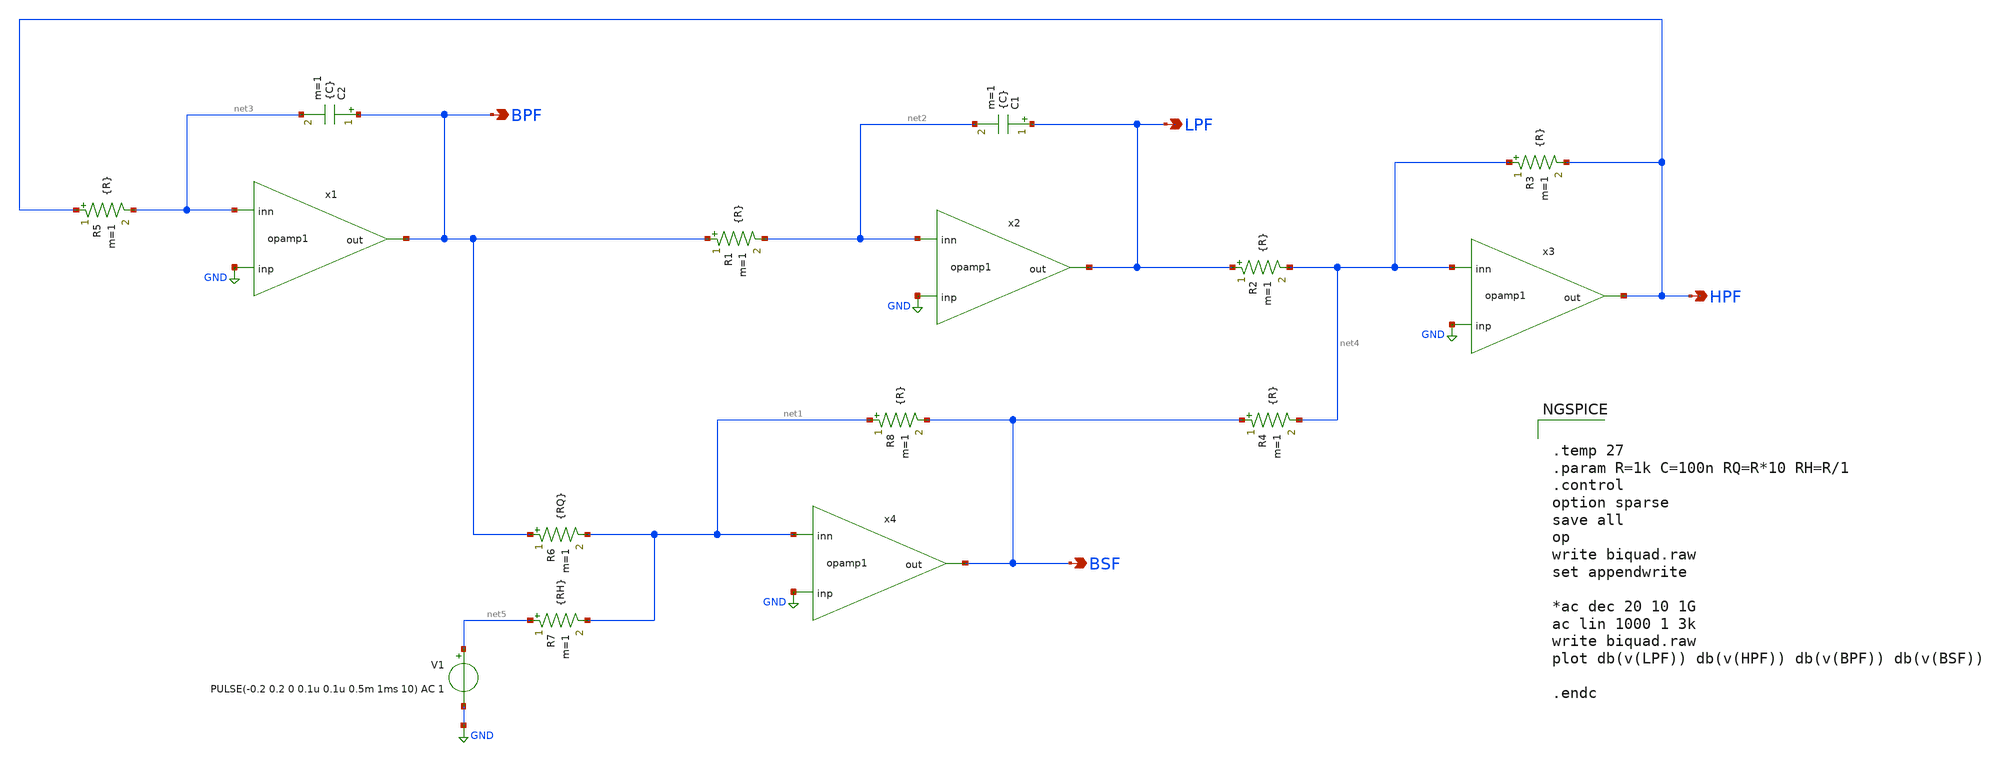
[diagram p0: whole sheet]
** sch_path: prj/template/2_Idealized_circuits/biquad_univ.sch
**.subckt biquad_univ HPF BSF LPF BPF
*.opin HPF
*.opin BSF
*.opin LPF
*.opin BPF
C1 LPF net2 {C} m=1
C2 BPF net3 {C} m=1
R1 BPF net2 {R} m=1
R2 LPF net4 {R} m=1
R3 net4 HPF {R} m=1
R4 BSF net4 {R} m=1
R5 HPF net3 {R} m=1
R6 BPF net1 {RQ} m=1
R7 net5 net1 {RH} m=1
R8 net1 BSF {R} m=1
x1 GND net3 BPF opamp1
x2 GND net2 LPF opamp1
x3 GND net4 HPF opamp1
x4 GND net1 BSF opamp1
V1 net5 GND PULSE(-0.2 0.2 0 0.1u 0.1u 0.5m 1ms 10) AC 1
**** begin user architecture code


.temp 27
.param R=1k C=100n RQ=R*10 RH=R/1
.control
option sparse
save all
op
write biquad.raw
set appendwrite

*ac dec 20 10 1G
ac lin 1000 1 3k
write biquad.raw
plot db(v(LPF)) db(v(HPF)) db(v(BPF)) db(v(BSF))

.endc


**** end user architecture code
**.ends

* expanding   symbol:  opamp1.sym # of pins=3
** sym_path: prj/template/2_Idealized_circuits/opamp1.sym
** sch_path: prj/template/2_Idealized_circuits/opamp1.sch
.subckt opamp1 inp inn out
*.ipin inp
*.ipin inn
*.opin out
Rin inp inn 10MEG m=1
Rout net2 out 10 m=1
Cp net1 GND 1.59u m=1
Rp GND net1 1k m=1
Ebuf net2 GND net1 GND 1
G1 net1 GND inp inn 1
.ends

.GLOBAL GND
.end
